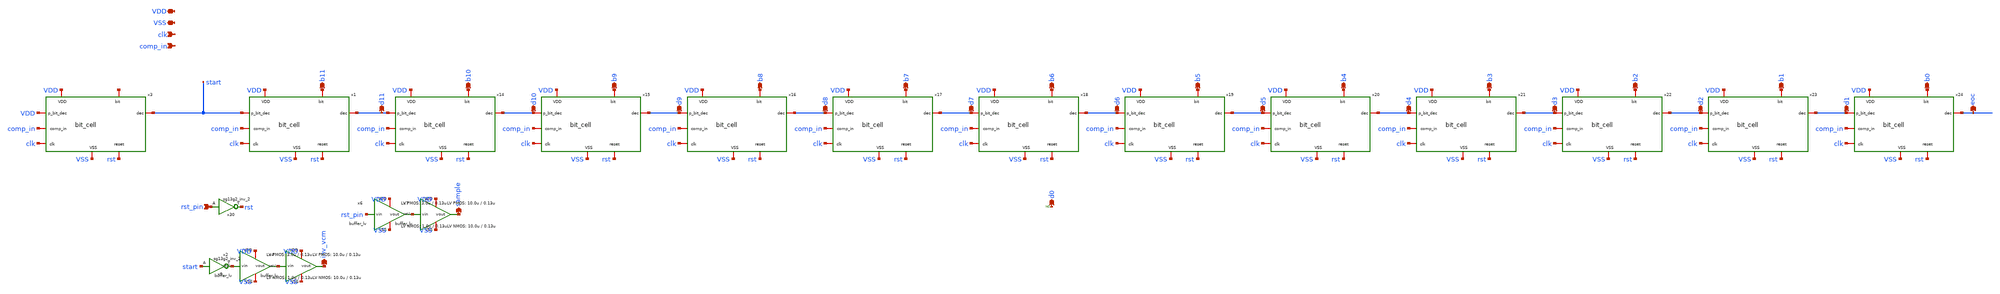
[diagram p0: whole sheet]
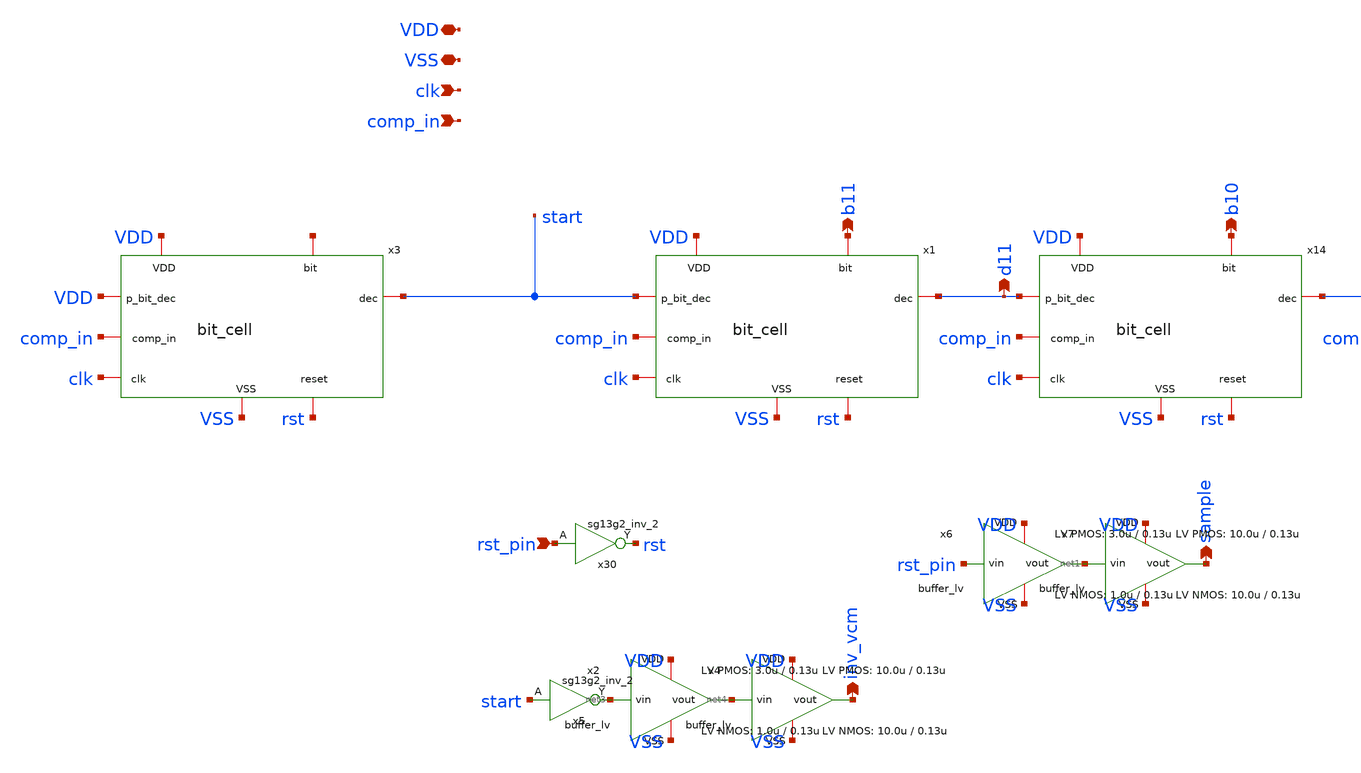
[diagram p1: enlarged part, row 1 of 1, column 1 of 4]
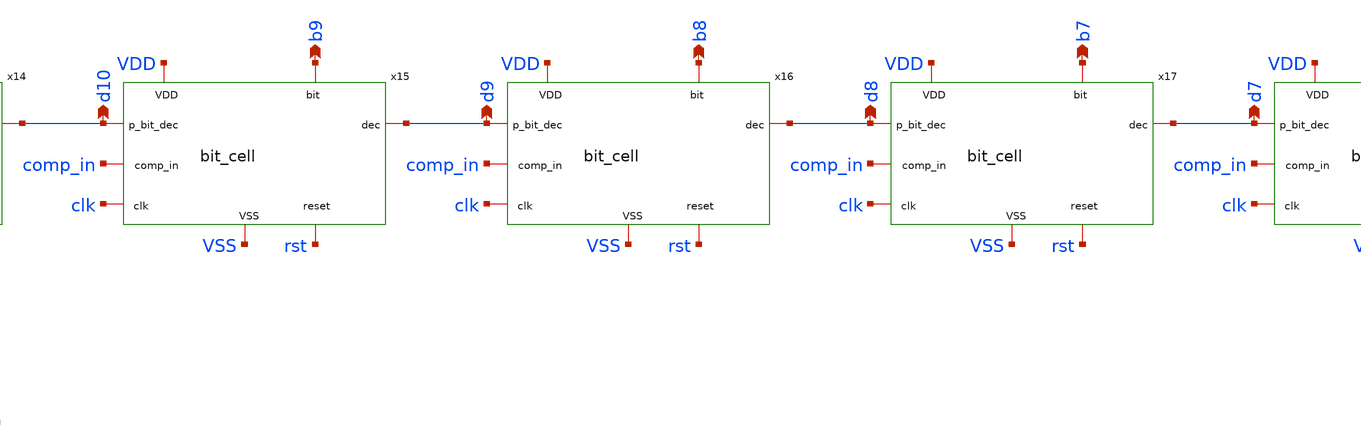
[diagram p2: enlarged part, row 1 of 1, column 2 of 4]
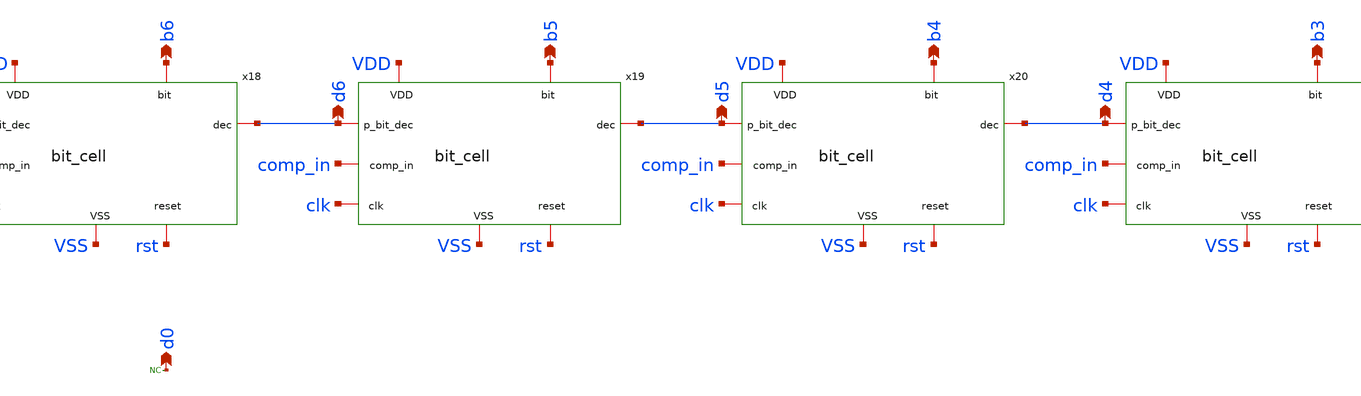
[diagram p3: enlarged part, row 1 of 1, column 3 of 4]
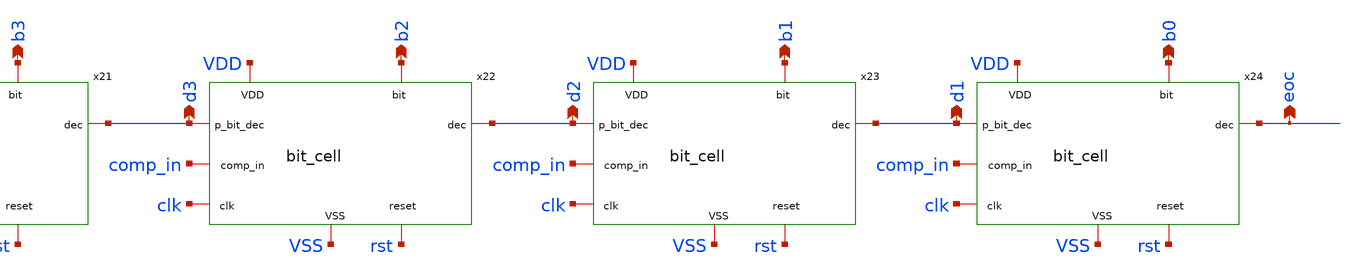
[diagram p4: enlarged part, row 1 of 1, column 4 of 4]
** sch_path: xschem/logic/logic.sch
**.subckt logic VDD VSS clk comp_in b0 d0 b1 d1 b2 d2 b3 d3 b4 d4 b5 d5 b6 d6 b7 d7 b8 d8 b9 d9 b10
*+ d10 b11 d11 rst_pin eoc sample inv_vcm
*.iopin VDD
*.iopin VSS
*.ipin clk
*.ipin comp_in
*.opin b0
*.opin d0
*.opin b1
*.opin d1
*.opin b2
*.opin d2
*.opin b3
*.opin d3
*.opin b4
*.opin d4
*.opin b5
*.opin d5
*.opin b6
*.opin d6
*.opin b7
*.opin d7
*.opin b8
*.opin d8
*.opin b9
*.opin d9
*.opin b10
*.opin d10
*.opin b11
*.opin d11
*.ipin rst_pin
*.opin eoc
*.opin sample
*.opin inv_vcm
x1 clk start rst comp_in VDD b11 VSS d11 bit_cell
x14 clk d11 rst comp_in VDD b10 VSS d10 bit_cell
x15 clk d10 rst comp_in VDD b9 VSS d9 bit_cell
x16 clk d9 rst comp_in VDD b8 VSS d8 bit_cell
x17 clk d8 rst comp_in VDD b7 VSS d7 bit_cell
x18 clk d7 rst comp_in VDD b6 VSS d6 bit_cell
x19 clk d6 rst comp_in VDD b5 VSS d5 bit_cell
x20 clk d5 rst comp_in VDD b4 VSS d4 bit_cell
x21 clk d4 rst comp_in VDD b3 VSS d3 bit_cell
x22 clk d3 rst comp_in VDD b2 VSS d2 bit_cell
x23 clk d2 rst comp_in VDD b1 VSS d1 bit_cell
x24 clk d1 rst comp_in VDD b0 VSS eoc bit_cell
x6 VDD rst_pin net1 VSS buffer_lv W_P_INV=3.0u L_P_INV=0.13u W_N_INV=1.0u L_N_INV=0.13u
x7 VDD net1 sample VSS buffer_lv W_P_INV=10.0u L_P_INV=0.13u W_N_INV=10.0u L_N_INV=0.13u
x30 rst rst_pin VDD VSS sg13g2_inv_2
x3 clk VDD rst comp_in VDD net2 VSS start bit_cell
* noconn d0
x2 VDD net3 net4 VSS buffer_lv W_P_INV=3.0u L_P_INV=0.13u W_N_INV=1.0u L_N_INV=0.13u
x4 VDD net4 inv_vcm VSS buffer_lv W_P_INV=10.0u L_P_INV=0.13u W_N_INV=10.0u L_N_INV=0.13u
x5 net3 start VDD VSS sg13g2_inv_2
**.ends
.end
